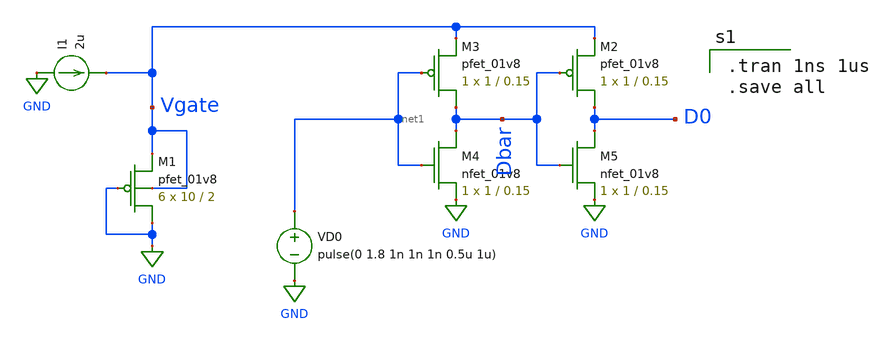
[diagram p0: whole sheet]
** sch_path: schematic/old/vgate_data_input.sch
**.subckt vgate_data_input
XM1 GND GND Vgate Vgate sky130_fd_pr__pfet_01v8 L=2 W=10 nf=1 ad='int((nf+1)/2) * W/nf * 0.29' as='int((nf+2)/2) * W/nf * 0.29'
+ pd='2*int((nf+1)/2) * (W/nf + 0.29)' ps='2*int((nf+2)/2) * (W/nf + 0.29)' nrd='0.29 / W' nrs='0.29 / W'
+ sa=0 sb=0 sd=0 mult=6 m=6
I1 GND Vgate 2u
XM3 Dbar net1 Vgate VDD sky130_fd_pr__pfet_01v8 L=0.15 W=1 nf=1 ad='int((nf+1)/2) * W/nf * 0.29' as='int((nf+2)/2) * W/nf * 0.29'
+ pd='2*int((nf+1)/2) * (W/nf + 0.29)' ps='2*int((nf+2)/2) * (W/nf + 0.29)' nrd='0.29 / W' nrs='0.29 / W'
+ sa=0 sb=0 sd=0 mult=1 m=1
XM4 Dbar net1 GND GND sky130_fd_pr__nfet_01v8 L=0.15 W=1 nf=1 ad='int((nf+1)/2) * W/nf * 0.29' as='int((nf+2)/2) * W/nf * 0.29'
+ pd='2*int((nf+1)/2) * (W/nf + 0.29)' ps='2*int((nf+2)/2) * (W/nf + 0.29)' nrd='0.29 / W' nrs='0.29 / W'
+ sa=0 sb=0 sd=0 mult=1 m=1
VD0 net1 GND pulse(0 1.8 1n 1n 1n 0.5u 1u)
XM2 D0 Dbar Vgate VDD sky130_fd_pr__pfet_01v8 L=0.15 W=1 nf=1 ad='int((nf+1)/2) * W/nf * 0.29' as='int((nf+2)/2) * W/nf * 0.29'
+ pd='2*int((nf+1)/2) * (W/nf + 0.29)' ps='2*int((nf+2)/2) * (W/nf + 0.29)' nrd='0.29 / W' nrs='0.29 / W'
+ sa=0 sb=0 sd=0 mult=1 m=1
XM5 D0 Dbar GND GND sky130_fd_pr__nfet_01v8 L=0.15 W=1 nf=1 ad='int((nf+1)/2) * W/nf * 0.29' as='int((nf+2)/2) * W/nf * 0.29'
+ pd='2*int((nf+1)/2) * (W/nf + 0.29)' ps='2*int((nf+2)/2) * (W/nf + 0.29)' nrd='0.29 / W' nrs='0.29 / W'
+ sa=0 sb=0 sd=0 mult=1 m=1
**** begin user architecture code

.option wnflag=1
.param MC_SWITCH=0.0
.lib ~/skywater/skywater-pdk/libraries/sky130_fd_pr_ngspice/latest/models/sky130.lib.spice tt


.tran 1ns 1us
.save all

**** end user architecture code
**.ends
.GLOBAL GND
.end
